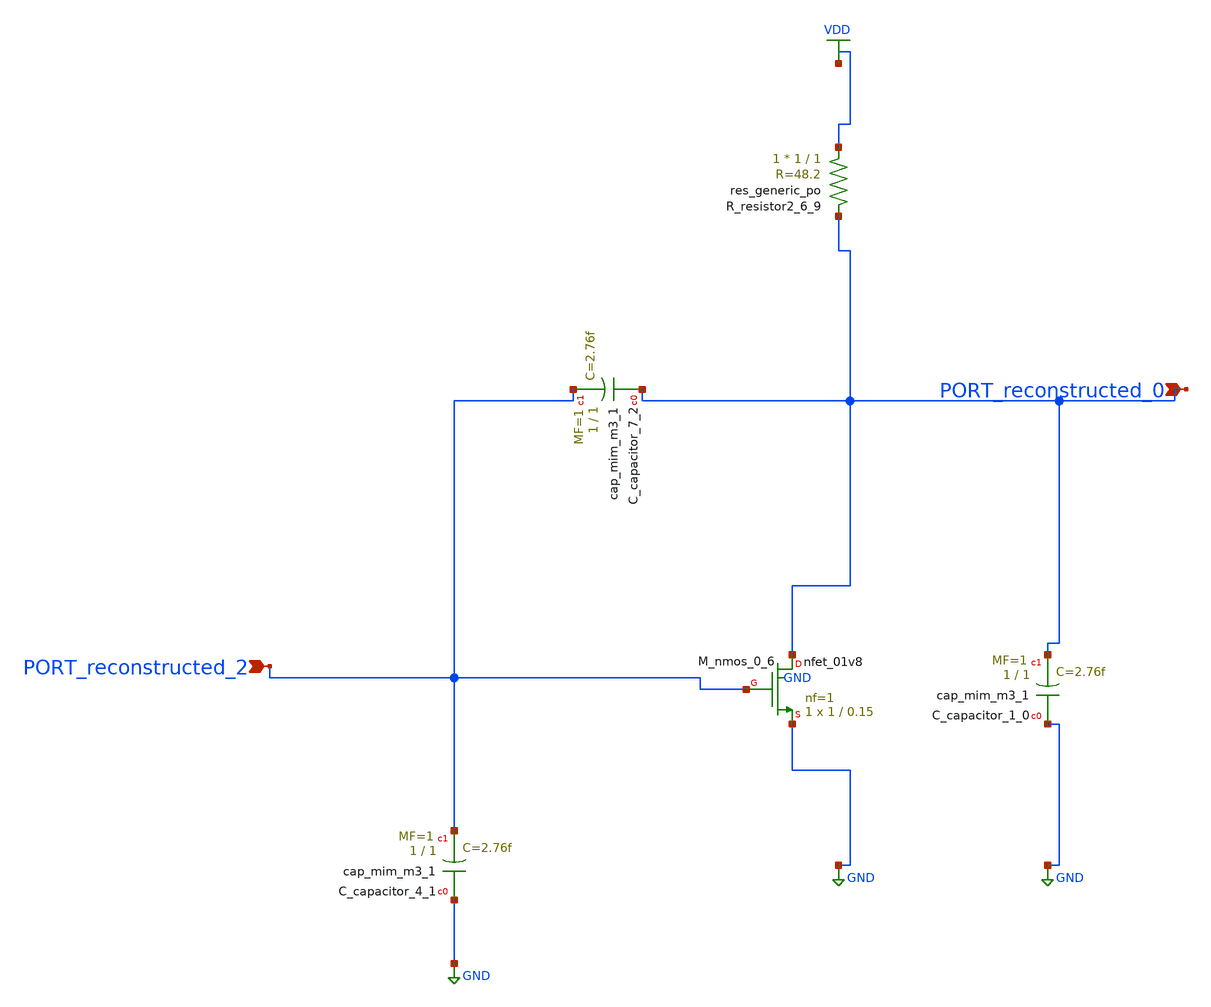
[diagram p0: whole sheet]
** sch_path: schematics/AMSNet/385.sch
**.subckt 385 PORT_reconstructed_2 PORT_reconstructed_0
*.ipin PORT_reconstructed_2
*.ipin PORT_reconstructed_0
XC_capacitor_1_0 GND PORT_reconstructed_0 sky130_fd_pr__cap_mim_m3_1 W=1 L=1 MF=1 m=1
XC_capacitor_4_1 GND PORT_reconstructed_2 sky130_fd_pr__cap_mim_m3_1 W=1 L=1 MF=1 m=1
XC_capacitor_7_2 PORT_reconstructed_0 PORT_reconstructed_2 sky130_fd_pr__cap_mim_m3_1 W=1 L=1 MF=1
+ m=1
XM_nmos_0_6 PORT_reconstructed_0 PORT_reconstructed_2 GND GND sky130_fd_pr__nfet_01v8 L=0.15 W=1 nf=1
+ ad='int((1 + 1)/2) * 1 / 1 * 0.29' as='int((1 + 2)/2) * 1 / 1 * 0.29' pd='2*int((1 + 1)/2) * (1 / 1 + 0.29)'
+ ps='2*int((1 + 2)/2) * (1 / 1 + 0.29)' nrd='0.29 / 1 ' nrs='0.29 / 1 ' sa=0 sb=0 sd=0 mult=1 m=1
XR_resistor2_6_9 VDD PORT_reconstructed_0 sky130_fd_pr__res_generic_po W=1 L=1 m=1
**.ends
.GLOBAL GND
.GLOBAL VDD
.end
